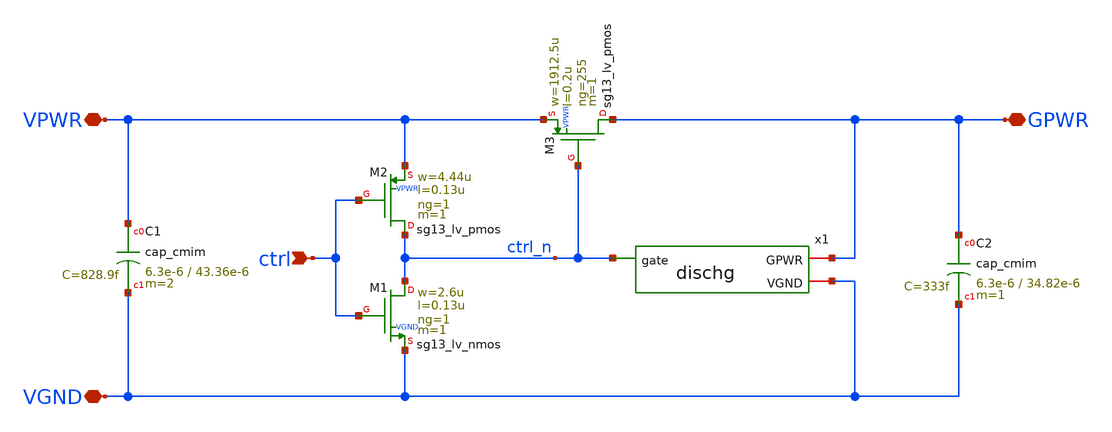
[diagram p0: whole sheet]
** sch_path: pg/ihp-sg13g2/tt_pg_1v5_ll_1/xschem/tt_pg_1v5_ll_1.sch
**.subckt tt_pg_1v5_ll_1 ctrl VPWR VGND GPWR
*.ipin ctrl
*.iopin VPWR
*.iopin VGND
*.iopin GPWR
XM1 ctrl_n ctrl VGND VGND sg13_lv_nmos w=2.6u l=0.13u ng=1 m=1
XM2 ctrl_n ctrl VPWR VPWR sg13_lv_pmos w=4.44u l=0.13u ng=1 m=1
XM3 GPWR ctrl_n VPWR VPWR sg13_lv_pmos w=1912.5u l=0.2u ng=255 m=1
XC1 VPWR VGND cap_cmim w=6.3e-6 l=43.36e-6 m=2 mm_ok=1
XC2 GPWR VGND cap_cmim w=6.3e-6 l=34.82e-6 m=1 mm_ok=1
x1 VGND GPWR ctrl_n dischg
**.ends

* expanding   symbol:  dischg.sym # of pins=3
** sym_path: pg/ihp-sg13g2/common/xschem/dischg.sym
** sch_path: pg/ihp-sg13g2/common/xschem/dischg.sch
.subckt dischg VGND GPWR gate
*.iopin GPWR
*.iopin VGND
*.ipin gate
XM1 GPWR gate net3 VGND sg13_lv_nmos w=0.50u l=0.65u ng=1 m=1
XM2 net3 gate net2 VGND sg13_lv_nmos w=0.50u l=0.65u ng=1 m=1
XM3 net2 gate net1 VGND sg13_lv_nmos w=0.50u l=0.65u ng=1 m=1
XM4 net1 gate VGND VGND sg13_lv_nmos w=0.50u l=0.65u ng=1 m=1
XM5 GPWR gate net6 VGND sg13_lv_nmos w=0.50u l=0.65u ng=1 m=1
XM6 net6 gate net5 VGND sg13_lv_nmos w=0.50u l=0.65u ng=1 m=1
XM7 net5 gate net4 VGND sg13_lv_nmos w=0.50u l=0.65u ng=1 m=1
XM8 net4 gate VGND VGND sg13_lv_nmos w=0.50u l=0.65u ng=1 m=1
.ends

.end
